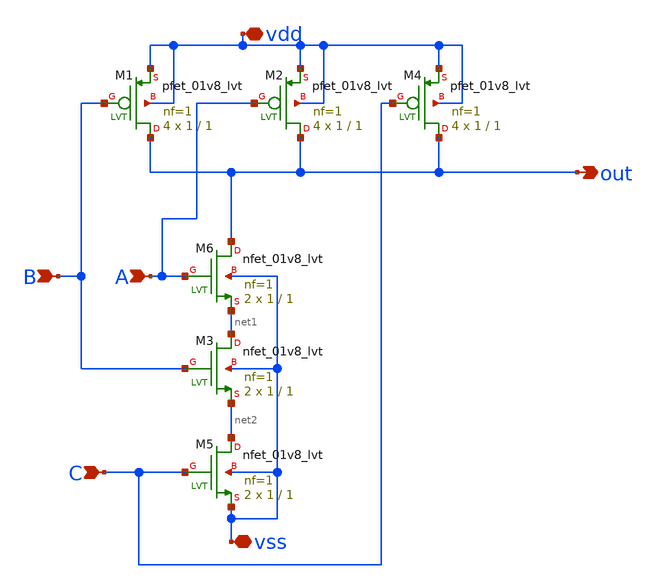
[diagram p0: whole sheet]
** sch_path: NAND.sch
**.subckt NAND vdd vss A C B out
*.iopin vdd
*.iopin vss
*.ipin A
*.ipin C
*.ipin B
*.opin out
XM6 out A net1 vss sky130_fd_pr__nfet_01v8_lvt L=1 W=1 nf=1 ad='int((1 + 1)/2) * 1 / 1 * 0.29' as='int((1 + 2)/2) * 1 / 1 * 0.29'
+ pd='2*int((1 + 1)/2) * (1 / 1 + 0.29)' ps='2*int((1 + 2)/2) * (1 / 1 + 0.29)' nrd='0.29 / 1 ' nrs='0.29 / 1 '
+ sa=0 sb=0 sd=0 mult=2 m=2
XM1 out B vdd vdd sky130_fd_pr__pfet_01v8_lvt L=1 W=1 nf=1 ad='int((1 + 1)/2) * 1 / 1 * 0.29' as='int((1 + 2)/2) * 1 / 1 * 0.29'
+ pd='2*int((1 + 1)/2) * (1 / 1 + 0.29)' ps='2*int((1 + 2)/2) * (1 / 1 + 0.29)' nrd='0.29 / 1 ' nrs='0.29 / 1 '
+ sa=0 sb=0 sd=0 mult=4 m=4
XM2 out A vdd vdd sky130_fd_pr__pfet_01v8_lvt L=1 W=1 nf=1 ad='int((1 + 1)/2) * 1 / 1 * 0.29' as='int((1 + 2)/2) * 1 / 1 * 0.29'
+ pd='2*int((1 + 1)/2) * (1 / 1 + 0.29)' ps='2*int((1 + 2)/2) * (1 / 1 + 0.29)' nrd='0.29 / 1 ' nrs='0.29 / 1 '
+ sa=0 sb=0 sd=0 mult=4 m=4
XM3 net1 B net2 vss sky130_fd_pr__nfet_01v8_lvt L=1 W=1 nf=1 ad='int((1 + 1)/2) * 1 / 1 * 0.29' as='int((1 + 2)/2) * 1 / 1 * 0.29'
+ pd='2*int((1 + 1)/2) * (1 / 1 + 0.29)' ps='2*int((1 + 2)/2) * (1 / 1 + 0.29)' nrd='0.29 / 1 ' nrs='0.29 / 1 '
+ sa=0 sb=0 sd=0 mult=2 m=2
XM4 out C vdd vdd sky130_fd_pr__pfet_01v8_lvt L=1 W=1 nf=1 ad='int((1 + 1)/2) * 1 / 1 * 0.29' as='int((1 + 2)/2) * 1 / 1 * 0.29'
+ pd='2*int((1 + 1)/2) * (1 / 1 + 0.29)' ps='2*int((1 + 2)/2) * (1 / 1 + 0.29)' nrd='0.29 / 1 ' nrs='0.29 / 1 '
+ sa=0 sb=0 sd=0 mult=4 m=4
XM5 net2 C vss vss sky130_fd_pr__nfet_01v8_lvt L=1 W=1 nf=1 ad='int((1 + 1)/2) * 1 / 1 * 0.29' as='int((1 + 2)/2) * 1 / 1 * 0.29'
+ pd='2*int((1 + 1)/2) * (1 / 1 + 0.29)' ps='2*int((1 + 2)/2) * (1 / 1 + 0.29)' nrd='0.29 / 1 ' nrs='0.29 / 1 '
+ sa=0 sb=0 sd=0 mult=2 m=2
**.ends
.end
